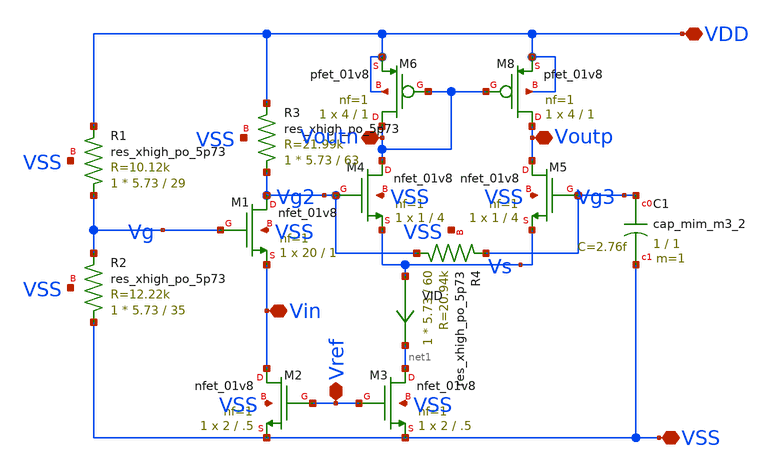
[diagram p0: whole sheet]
** sch_path: hw06/xschem/lna.sch
**.subckt lna VSS VDD Voutp Voutn Vref Vin
*.iopin VSS
*.iopin VDD
*.iopin Voutp
*.iopin Voutn
*.iopin Vref
*.iopin Vin
XR1 Vg VDD VSS sky130_fd_pr__res_xhigh_po_5p73 L=29 mult=1 m=1
XR2 VSS Vg VSS sky130_fd_pr__res_xhigh_po_5p73 L=35 mult=1 m=1
XM1 Vg2 Vg Vin VSS sky130_fd_pr__nfet_01v8 L=1 W=20 nf=1 ad='int((nf+1)/2) * W/nf * 0.29' as='int((nf+2)/2) * W/nf * 0.29'
+ pd='2*int((nf+1)/2) * (W/nf + 0.29)' ps='2*int((nf+2)/2) * (W/nf + 0.29)' nrd='0.29 / W' nrs='0.29 / W'
+ sa=0 sb=0 sd=0 mult=1 m=1
XM2 Vin Vref VSS VSS sky130_fd_pr__nfet_01v8 L=.5 W=2 nf=1 ad='int((nf+1)/2) * W/nf * 0.29' as='int((nf+2)/2) * W/nf * 0.29'
+ pd='2*int((nf+1)/2) * (W/nf + 0.29)' ps='2*int((nf+2)/2) * (W/nf + 0.29)' nrd='0.29 / W' nrs='0.29 / W'
+ sa=0 sb=0 sd=0 mult=1 m=1
XM3 net1 Vref VSS VSS sky130_fd_pr__nfet_01v8 L=.5 W=2 nf=1 ad='int((nf+1)/2) * W/nf * 0.29' as='int((nf+2)/2) * W/nf * 0.29'
+ pd='2*int((nf+1)/2) * (W/nf + 0.29)' ps='2*int((nf+2)/2) * (W/nf + 0.29)' nrd='0.29 / W' nrs='0.29 / W'
+ sa=0 sb=0 sd=0 mult=1 m=1
XM4 Voutn Vg2 Vs VSS sky130_fd_pr__nfet_01v8 L=4 W=1 nf=1 ad='int((nf+1)/2) * W/nf * 0.29' as='int((nf+2)/2) * W/nf * 0.29'
+ pd='2*int((nf+1)/2) * (W/nf + 0.29)' ps='2*int((nf+2)/2) * (W/nf + 0.29)' nrd='0.29 / W' nrs='0.29 / W'
+ sa=0 sb=0 sd=0 mult=1 m=1
XM5 Voutp Vg3 Vs VSS sky130_fd_pr__nfet_01v8 L=4 W=1 nf=1 ad='int((nf+1)/2) * W/nf * 0.29' as='int((nf+2)/2) * W/nf * 0.29'
+ pd='2*int((nf+1)/2) * (W/nf + 0.29)' ps='2*int((nf+2)/2) * (W/nf + 0.29)' nrd='0.29 / W' nrs='0.29 / W'
+ sa=0 sb=0 sd=0 mult=1 m=1
XR3 Vg2 VDD VSS sky130_fd_pr__res_xhigh_po_5p73 L=63 mult=1 m=1
XR4 Vg2 Vg3 VSS sky130_fd_pr__res_xhigh_po_5p73 L=60 mult=1 m=1
VID Vs net1 0
.save i(vid)
XC1 Vg3 VSS sky130_fd_pr__cap_mim_m3_2 W=1 L=1 MF=1 m=1
XM8 Voutp Voutn VDD VDD sky130_fd_pr__pfet_01v8 L=1 W=4 nf=1 ad='int((nf+1)/2) * W/nf * 0.29' as='int((nf+2)/2) * W/nf * 0.29'
+ pd='2*int((nf+1)/2) * (W/nf + 0.29)' ps='2*int((nf+2)/2) * (W/nf + 0.29)' nrd='0.29 / W' nrs='0.29 / W'
+ sa=0 sb=0 sd=0 mult=1 m=1
XM6 Voutn Voutn VDD VDD sky130_fd_pr__pfet_01v8 L=1 W=4 nf=1 ad='int((nf+1)/2) * W/nf * 0.29' as='int((nf+2)/2) * W/nf * 0.29'
+ pd='2*int((nf+1)/2) * (W/nf + 0.29)' ps='2*int((nf+2)/2) * (W/nf + 0.29)' nrd='0.29 / W' nrs='0.29 / W'
+ sa=0 sb=0 sd=0 mult=1 m=1
**.ends
.end
